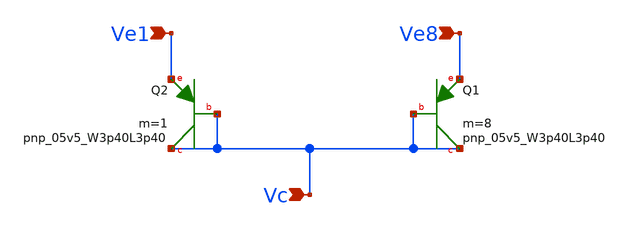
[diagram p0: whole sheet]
** sch_path: design/LELO_GR01_SKY130A/Diodes.sch
**.subckt Diodes Ve1 Ve8 Vc
*.ipin Ve1
*.ipin Ve8
*.ipin Vc
XQ1 Vc Vc Ve8 sky130_fd_pr__pnp_05v5_W3p40L3p40 m=8
XQ2 Vc Vc Ve1 sky130_fd_pr__pnp_05v5_W3p40L3p40 m=1
**.ends
.end
